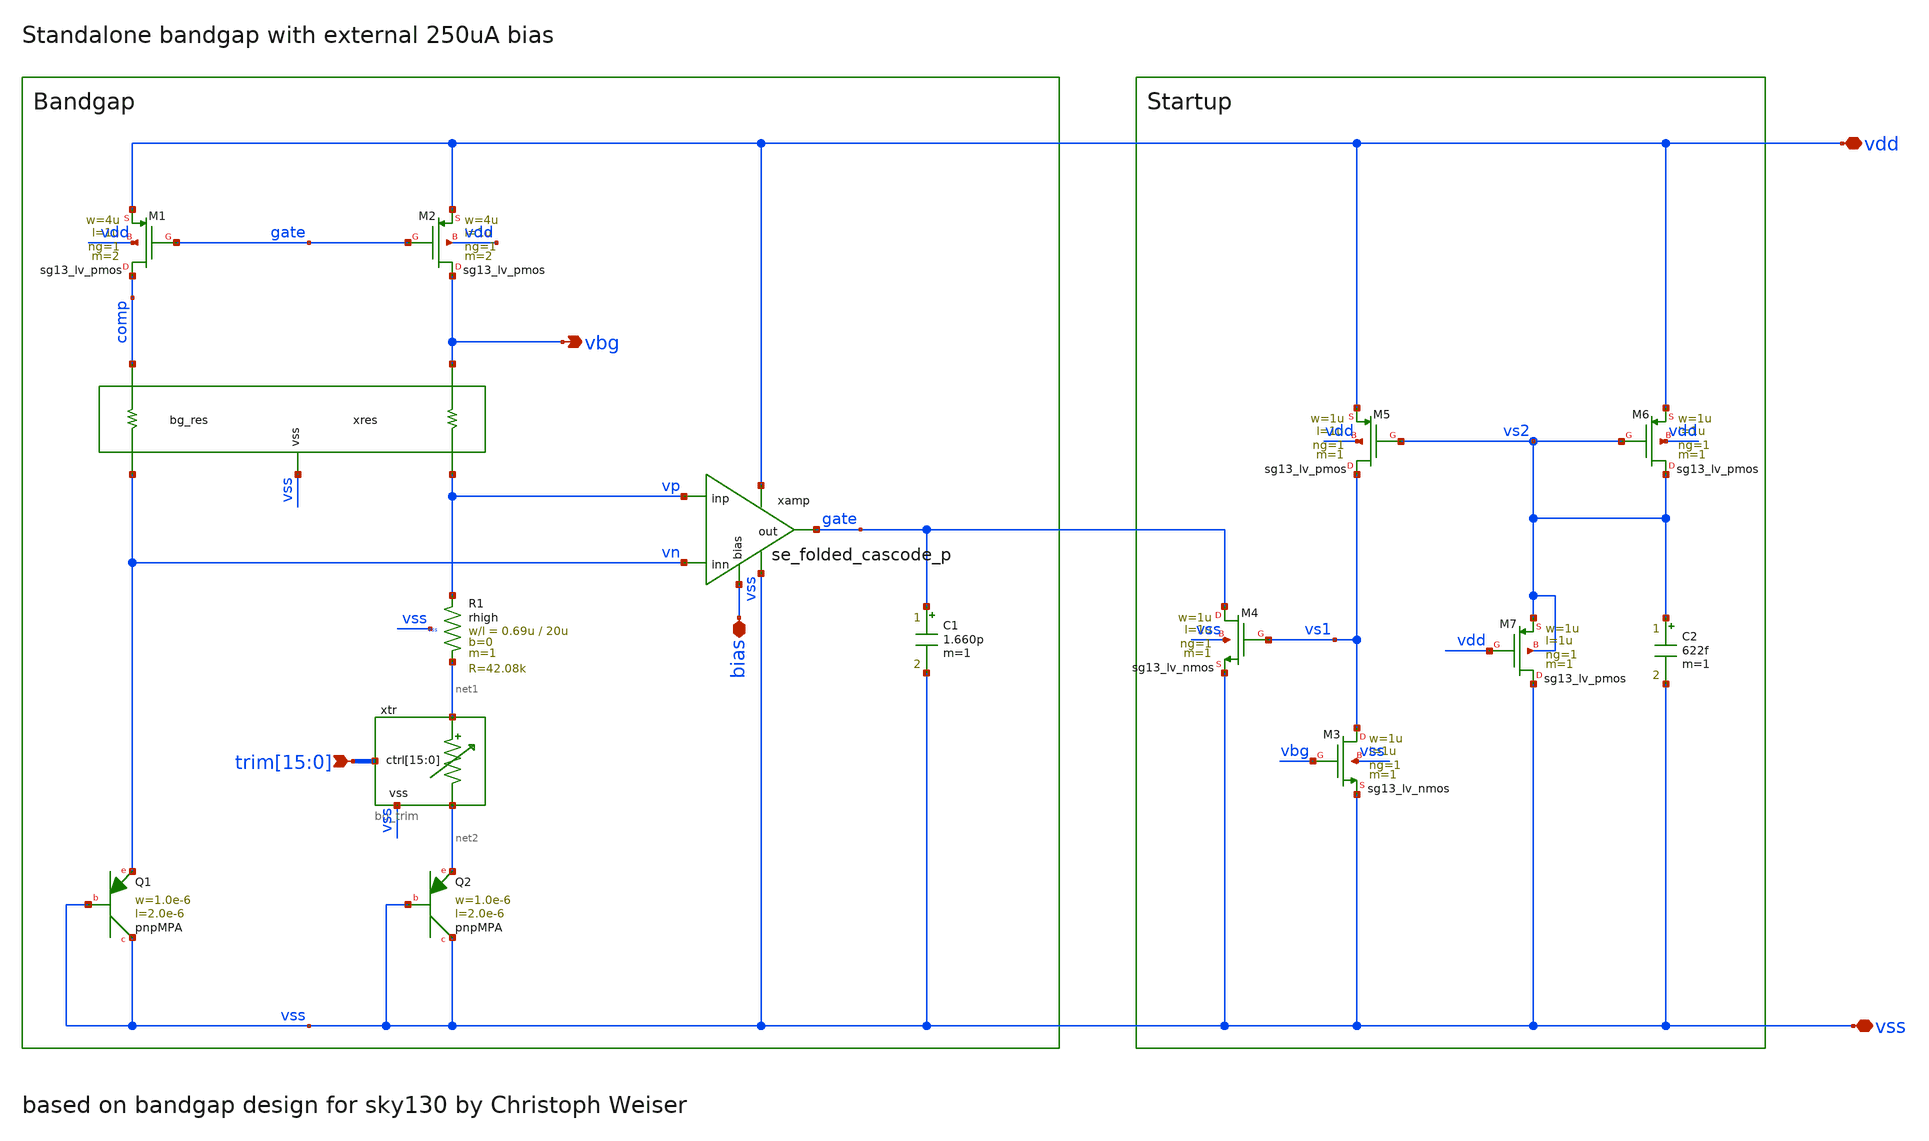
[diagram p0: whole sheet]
** sch_path: xschem/bandgap_orig/sg13cmos5l_ocd_ip__bandgap.sch
**.subckt sg13cmos5l_ocd_ip__bandgap vdd vss vbg bias
*+ trim[15],trim[14],trim[13],trim[12],trim[11],trim[10],trim[9],trim[8],trim[7],trim[6],trim[5],trim[4],trim[3],trim[2],trim[1],trim[0]
*.iopin vdd
*.iopin vss
*.opin vbg
*.iopin bias
*.ipin
*+ trim[15],trim[14],trim[13],trim[12],trim[11],trim[10],trim[9],trim[8],trim[7],trim[6],trim[5],trim[4],trim[3],trim[2],trim[1],trim[0]
XQ2 vss vss net2 pnpMPA a=2p p=6u m=8
XQ1 vss vss vn pnpMPA a=2p p=6u m=1
C1 gate vss 1.660p m=1
xres vbg comp vp vn vss bg_res
XR1 vp net1 vss rhigh w=0.69u l=20u m=1 b=0 mm_ok=1
XM1 comp gate vdd vdd sg13_lv_pmos w=4u l=1u ng=1 m=2 mm_ok=1
XM2 vbg gate vdd vdd sg13_lv_pmos w=4u l=1u ng=1 m=2 mm_ok=1
xtr net1 net2 trim[15] trim[14] trim[13] trim[12] trim[11] trim[10] trim[9] trim[8] trim[7] trim[6]
+ trim[5] trim[4] trim[3] trim[2] trim[1] trim[0] vss bg_trim
xamp vdd gate vp vn vss bias se_folded_cascode_p
XM3 vs1 vbg vss vss sg13_lv_nmos w=1u l=1u ng=1 m=1 mm_ok=1
XM4 gate vs1 vss vss sg13_lv_nmos w=1u l=1u ng=1 m=1 mm_ok=1
XM5 vs1 vs2 vdd vdd sg13_lv_pmos w=1u l=1u ng=1 m=1 mm_ok=1
C2 vs2 vss 622f m=1
XM6 vs2 vs2 vdd vdd sg13_lv_pmos w=1u l=1u ng=1 m=1 mm_ok=1
XM7 vss vdd vs2 vs2 sg13_lv_pmos w=1u l=1u ng=1 m=1 mm_ok=1
**.ends

* expanding   symbol:  bg_res.sym # of pins=5
** sym_path: bg_res.sym
** sch_path: bg_res.sch
.subckt bg_res b a d c vss
*.ipin a
*.ipin b
*.opin c
*.opin d
*.iopin vss
XR1 a net1 sub! rhigh w=0.69u l=20u m=1 b=0 mm_ok=1
XR2 b net2 vss rhigh w=0.69u l=20u m=1 b=0 mm_ok=1
XR3 net1 net6 vss rhigh w=0.69u l=20u m=1 b=0 mm_ok=1
XR4 net2 net5 vss rhigh w=0.69u l=20u m=1 b=0 mm_ok=1
XR5 net6 net3 vss rhigh w=0.69u l=20u m=1 b=0 mm_ok=1
XR6 net5 net4 vss rhigh w=0.69u l=20u m=1 b=0 mm_ok=1
XR7 net3 net10 vss rhigh w=0.69u l=20u m=1 b=0 mm_ok=1
XR8 net4 net9 vss rhigh w=0.69u l=20u m=1 b=0 mm_ok=1
XR9 net10 net7 vss rhigh w=0.69u l=20u m=1 b=0 mm_ok=1
XR10 net9 net8 vss rhigh w=0.69u l=20u m=1 b=0 mm_ok=1
XR11 net7 net12 vss rhigh w=0.69u l=20u m=1 b=0 mm_ok=1
XR12 net8 net11 vss rhigh w=0.69u l=20u m=1 b=0 mm_ok=1
XR13 net12 net14 vss rhigh w=0.69u l=20u m=1 b=0 mm_ok=1
XR14 net11 net13 vss rhigh w=0.69u l=20u m=1 b=0 mm_ok=1
XR15 net14 net16 vss rhigh w=0.69u l=20u m=1 b=0 mm_ok=1
XR16 net13 net15 vss rhigh w=0.69u l=20u m=1 b=0 mm_ok=1
XR17 net16 net18 vss rhigh w=0.69u l=20u m=1 b=0 mm_ok=1
XR18 net15 net17 vss rhigh w=0.69u l=20u m=1 b=0 mm_ok=1
XR19 net18 c vss rhigh w=0.69u l=20u m=1 b=0 mm_ok=1
XR20 net17 d vss rhigh w=0.69u l=20u m=1 b=0 mm_ok=1
.ends


* expanding   symbol:  bg_trim.sym # of pins=4
** sym_path: xschem/bg_trim.sym
** sch_path: xschem/bg_trim.sch
.subckt bg_trim top bot ctrl[15] ctrl[14] ctrl[13] ctrl[12] ctrl[11] ctrl[10] ctrl[9] ctrl[8]
+ ctrl[7] ctrl[6] ctrl[5] ctrl[4] ctrl[3] ctrl[2] ctrl[1] ctrl[0] vss
*.iopin vss
*.ipin
*+ ctrl[15],ctrl[14],ctrl[13],ctrl[12],ctrl[11],ctrl[10],ctrl[9],ctrl[8],ctrl[7],ctrl[6],ctrl[5],ctrl[4],ctrl[3],ctrl[2],ctrl[1],ctrl[0]
*.iopin bot
*.iopin top
XM0 net1 ctrl[0] bot vss sg13_hv_nmos w=2u l=0.5u ng=1 m=1 mm_ok=1
XM1 net2 ctrl[1] bot vss sg13_hv_nmos w=2u l=0.5u ng=1 m=1 mm_ok=1
XM2 net3 ctrl[2] bot vss sg13_hv_nmos w=2u l=0.5u ng=1 m=1 mm_ok=1
XM3 net4 ctrl[3] bot vss sg13_hv_nmos w=2u l=0.5u ng=1 m=1 mm_ok=1
XM4 net5 ctrl[4] bot vss sg13_hv_nmos w=2u l=0.5u ng=1 m=1 mm_ok=1
XM5 net6 ctrl[5] bot vss sg13_hv_nmos w=2u l=0.5u ng=1 m=1 mm_ok=1
XM6 net7 ctrl[6] bot vss sg13_hv_nmos w=2u l=0.5u ng=1 m=1 mm_ok=1
XM7 net8 ctrl[7] bot vss sg13_hv_nmos w=2u l=0.5u ng=1 m=1 mm_ok=1
XM12 net9 ctrl[12] bot vss sg13_hv_nmos w=2u l=0.5u ng=1 m=1 mm_ok=1
XM13 net11 ctrl[13] bot vss sg13_hv_nmos w=2u l=0.5u ng=1 m=1 mm_ok=1
XM14 net12 ctrl[14] bot vss sg13_hv_nmos w=2u l=0.5u ng=1 m=1 mm_ok=1
XM15 top ctrl[15] bot vss sg13_hv_nmos w=2u l=0.5u ng=1 m=1 mm_ok=1
XM8 net13 ctrl[8] bot vss sg13_hv_nmos w=2u l=0.5u ng=1 m=1 mm_ok=1
XM9 net14 ctrl[9] bot vss sg13_hv_nmos w=2u l=0.5u ng=1 m=1 mm_ok=1
XM10 net15 ctrl[10] bot vss sg13_hv_nmos w=2u l=0.5u ng=1 m=1 mm_ok=1
XM11 net10 ctrl[11] bot vss sg13_hv_nmos w=2u l=0.5u ng=1 m=1 mm_ok=1
XM16 vss vss vss vss sg13_hv_nmos w=2u l=0.5u ng=1 m=2 mm_ok=1
XR19 top net12 vss rppd w=1.41u l=3.4u m=1 b=0 mm_ok=1
XR1 net12 net11 vss rppd w=1.41u l=3.4u m=1 b=0 mm_ok=1
XR2 net11 net9 vss rppd w=1.41u l=3.4u m=1 b=0 mm_ok=1
XR3 net9 net10 vss rppd w=1.41u l=3.4u m=1 b=0 mm_ok=1
XR4 net10 net15 vss rppd w=1.41u l=3.4u m=1 b=0 mm_ok=1
XR5 net15 net14 vss rppd w=1.41u l=3.4u m=1 b=0 mm_ok=1
XR6 net14 net13 vss rppd w=1.41u l=3.4u m=1 b=0 mm_ok=1
XR7 net13 net8 vss rppd w=1.41u l=3.4u m=1 b=0 mm_ok=1
XR8 net8 net7 vss rppd w=1.41u l=3.4u m=1 b=0 mm_ok=1
XR9 net7 net6 vss rppd w=1.41u l=3.4u m=1 b=0 mm_ok=1
XR10 net6 net5 vss rppd w=1.41u l=3.4u m=1 b=0 mm_ok=1
XR11 net5 net4 vss rppd w=1.41u l=3.4u m=1 b=0 mm_ok=1
XR12 net4 net3 vss rppd w=1.41u l=3.4u m=1 b=0 mm_ok=1
XR13 net3 net2 vss rppd w=1.41u l=3.4u m=1 b=0 mm_ok=1
XR14 net2 net1 vss rppd w=1.41u l=3.4u m=1 b=0 mm_ok=1
XR15 net1 bot vss rppd w=1.41u l=3.4u m=1 b=0 mm_ok=1
XR16 vss vss vss rppd w=1.41u l=3.4u m=1 b=0 mm_ok=1
XR17 top top vss rppd w=1.41u l=3.4u m=1 b=0 mm_ok=1
.ends


* expanding   symbol:  se_folded_cascode_p.sym # of pins=6
** sym_path: se_folded_cascode_p.sym
** sch_path: se_folded_cascode_p.sch
.subckt se_folded_cascode_p vdd out inp inn vss bias
*.ipin inn
*.ipin inp
*.opin out
*.iopin bias
*.iopin vdd
*.iopin vss
XM3 out1p inn diff vdd sg13_lv_pmos w=4u l=1u ng=1 m=8 mm_ok=1
XM2 out1n inp diff vdd sg13_lv_pmos w=4u l=1u ng=1 m=8 mm_ok=1
XM1 diff vbp1 vdd vdd sg13_lv_pmos w=1u l=1u ng=1 m=16 mm_ok=1
XM4 out1n vbn1 vss vss sg13_lv_nmos w=1u l=1u ng=1 m=16 mm_ok=1
XM5 out1p vbn1 vss vss sg13_lv_nmos w=1u l=1u ng=1 m=16 mm_ok=1
XM6 mirr vbn2 out1n vss sg13_lv_nmos w=1u l=4u ng=1 m=8 mm_ok=1
XM7 out vbn2 out1p vss sg13_lv_nmos w=1u l=4u ng=1 m=8 mm_ok=1
XM8 mirr bias nd10 vdd sg13_lv_pmos w=2u l=4u ng=1 m=8 mm_ok=1
XM9 out bias nd11 vdd sg13_lv_pmos w=2u l=4u ng=1 m=8 mm_ok=1
XM10 nd10 mirr vdd vdd sg13_lv_pmos w=2u l=4u ng=1 m=8 mm_ok=1
XM11 nd11 mirr vdd vdd sg13_lv_pmos w=2u l=4u ng=1 m=8 mm_ok=1
XMB1 bias bias vbp1 vdd sg13_lv_pmos w=2u l=4u ng=1 m=4 mm_ok=1
XMB2 vbp1 vbp1 vdd vdd sg13_lv_pmos w=1u l=1u ng=1 m=4 mm_ok=1
XMB3 vbn2 vbp1 vdd vdd sg13_lv_pmos w=1u l=1u ng=1 m=4 mm_ok=1
XMB4 vbn2 vbn2 vbn1 vss sg13_lv_nmos w=1u l=4u ng=1 m=4 mm_ok=1
XMB5 vbn1 vbn1 vss vss sg13_lv_nmos w=1u l=1u ng=1 m=4 mm_ok=1
XMDUM1 vdd vdd vdd vdd sg13_lv_pmos w=2u l=4u ng=1 m=42 mm_ok=1
XMDUM2 mirr mirr mirr vdd sg13_lv_pmos w=2u l=4u ng=1 m=4 mm_ok=1
XMDUM3 bias bias bias vdd sg13_lv_pmos w=2u l=4u ng=1 m=4 mm_ok=1
XMDUM4 vss vss vss vss sg13_lv_nmos w=1u l=4u ng=1 m=24 mm_ok=1
XMDUM5 vbn2 vbn2 vbn2 vss sg13_lv_nmos w=1u l=4u ng=1 m=4 mm_ok=1
XMDUM6 vss vss vss vss sg13_lv_nmos w=1u l=1u ng=1 m=44 mm_ok=1
XMDUM7 diff diff diff vdd sg13_lv_pmos w=4u l=1u ng=1 m=4 mm_ok=1
.ends

.end
